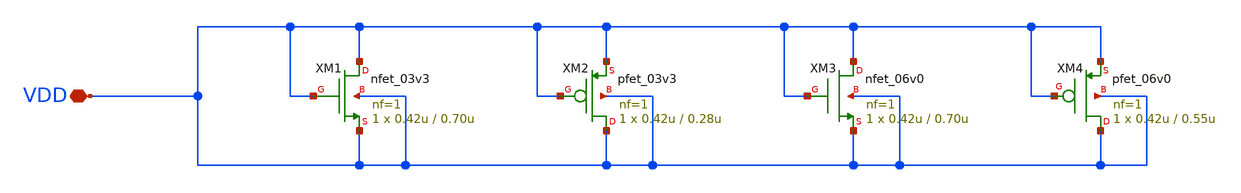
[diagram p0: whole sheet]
** sch_path: gf180mcuD/schematic/xschem/gf180_short1.sch
**.subckt gf180_short1 VDD
*.iopin VDD
XM1 VDD VDD VDD VDD nfet_03v3 L=0.70u W=0.42u nf=1 ad='int((nf+1)/2) * W/nf * 0.18u' as='int((nf+2)/2) * W/nf * 0.18u'
+ pd='2*int((nf+1)/2) * (W/nf + 0.18u)' ps='2*int((nf+2)/2) * (W/nf + 0.18u)' nrd='0.18u / W' nrs='0.18u / W'
+ sa=0 sb=0 sd=0 m=1 par=1
XM2 VDD VDD VDD VDD pfet_03v3 L=0.28u W=0.42u nf=1 ad='int((nf+1)/2) * W/nf * 0.18u' as='int((nf+2)/2) * W/nf * 0.18u'
+ pd='2*int((nf+1)/2) * (W/nf + 0.18u)' ps='2*int((nf+2)/2) * (W/nf + 0.18u)' nrd='0.18u / W' nrs='0.18u / W'
+ sa=0 sb=0 sd=0 m=1 par=1
XM3 VDD VDD VDD VDD nfet_06v0 L=0.70u W=0.42u nf=1 ad='int((nf+1)/2) * W/nf * 0.18u' as='int((nf+2)/2) * W/nf * 0.18u'
+ pd='2*int((nf+1)/2) * (W/nf + 0.18u)' ps='2*int((nf+2)/2) * (W/nf + 0.18u)' nrd='0.18u / W' nrs='0.18u / W'
+ sa=0 sb=0 sd=0 m=1 par=1
XM4 VDD VDD VDD VDD pfet_06v0 L=0.55u W=0.42u nf=1 ad='int((nf+1)/2) * W/nf * 0.18u' as='int((nf+2)/2) * W/nf * 0.18u'
+ pd='2*int((nf+1)/2) * (W/nf + 0.18u)' ps='2*int((nf+2)/2) * (W/nf + 0.18u)' nrd='0.18u / W' nrs='0.18u / W'
+ sa=0 sb=0 sd=0 m=1
**.ends
.end
